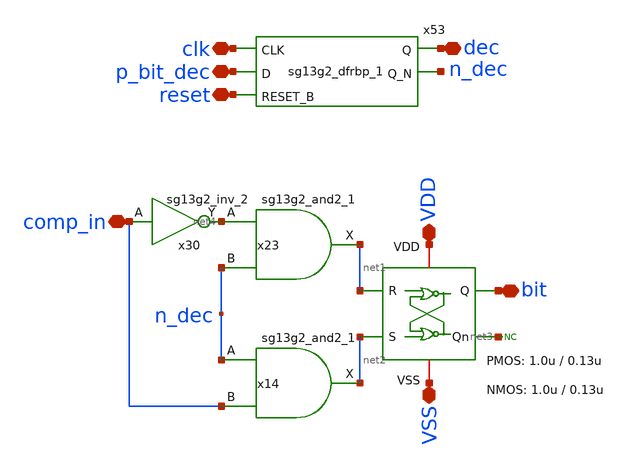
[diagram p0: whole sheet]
** sch_path: xschem/logic/bit_cell.sch
**.subckt bit_cell p_bit_dec clk reset comp_in VDD VSS bit dec
*.iopin p_bit_dec
*.iopin clk
*.iopin reset
*.iopin comp_in
*.iopin VDD
*.iopin VSS
*.iopin bit
*.iopin dec
x1 VDD net2 net3 VSS bit net1 SR_latch W_P_SR=1.0u L_P_SR=0.13u W_N_SR=1.0u L_N_SR=0.13u
x23 net1 net4 n_dec VDD VSS sg13g2_and2_1
x14 net2 n_dec comp_in VDD VSS sg13g2_and2_1
x30 net4 comp_in VDD VSS sg13g2_inv_2
x53 dec n_dec clk p_bit_dec reset VDD VSS sg13g2_dfrbp_1
* noconn #net3
**.ends
.end
